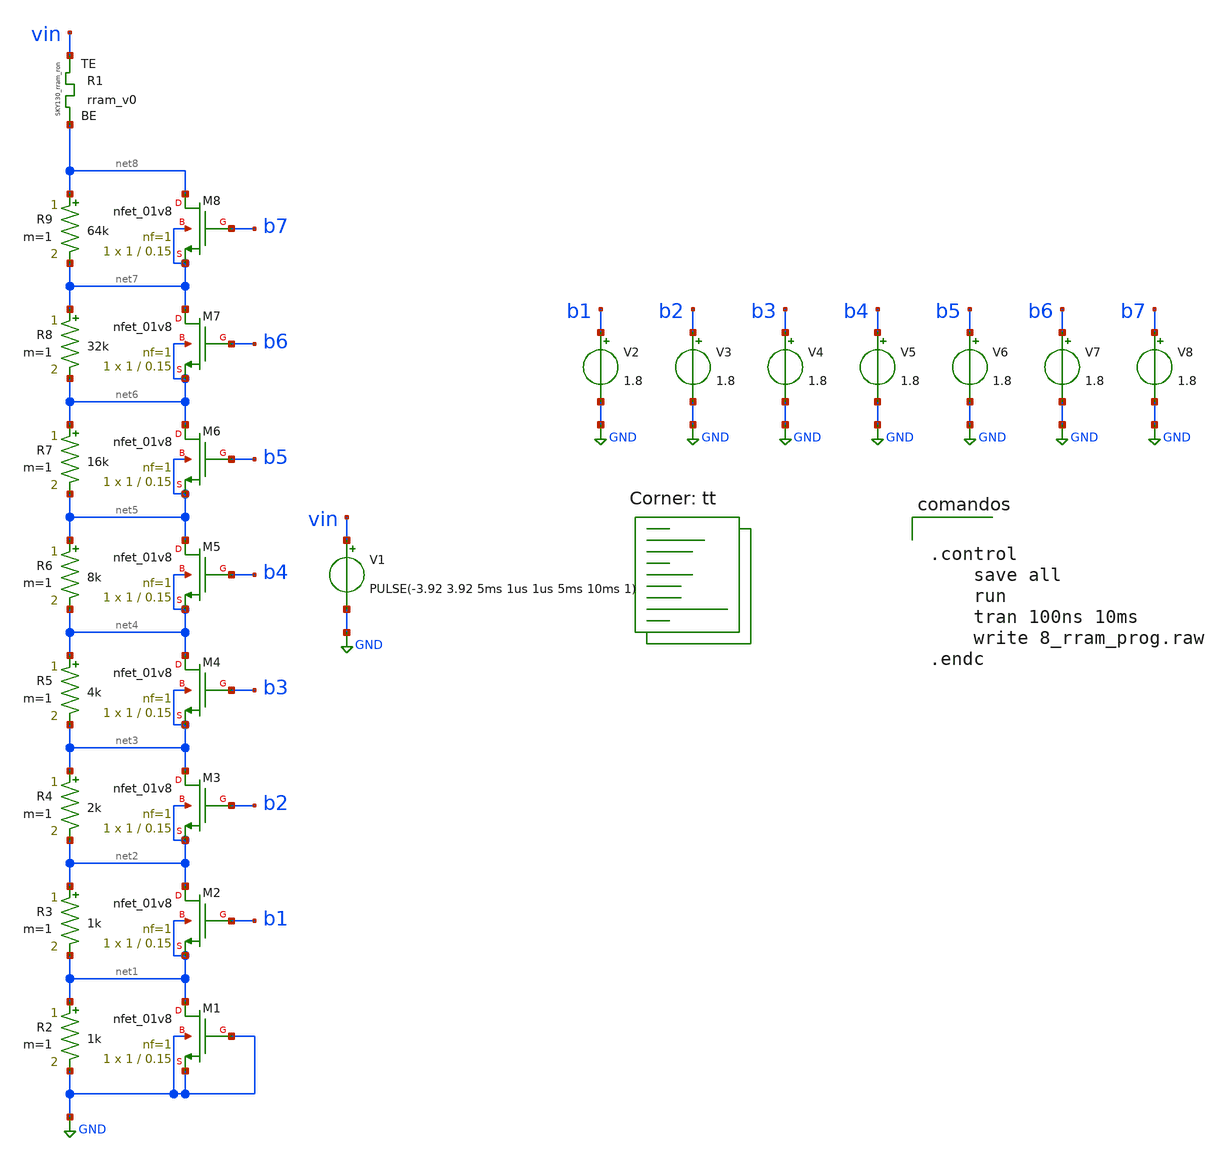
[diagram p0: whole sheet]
** sch_path: rram_programming/8_rram_prog.sch
**.subckt 8_rram_prog
V1 vin GND PULSE(-3.92 3.92 5ms 1us 1us 5ms 10ms 1)
XM1 net1 GND GND GND sky130_fd_pr__nfet_01v8 L=0.15 W=1 nf=1 ad='int((nf+1)/2) * W/nf * 0.29' as='int((nf+2)/2) * W/nf * 0.29'
+ pd='2*int((nf+1)/2) * (W/nf + 0.29)' ps='2*int((nf+2)/2) * (W/nf + 0.29)' nrd='0.29 / W' nrs='0.29 / W'
+ sa=0 sb=0 sd=0 mult=1 m=1
XR1 vin net8 rram_v0
R2 net1 GND 1k m=1
XM2 net2 b1 net1 net1 sky130_fd_pr__nfet_01v8 L=0.15 W=1 nf=1 ad='int((nf+1)/2) * W/nf * 0.29' as='int((nf+2)/2) * W/nf * 0.29'
+ pd='2*int((nf+1)/2) * (W/nf + 0.29)' ps='2*int((nf+2)/2) * (W/nf + 0.29)' nrd='0.29 / W' nrs='0.29 / W'
+ sa=0 sb=0 sd=0 mult=1 m=1
R3 net2 net1 1k m=1
XM3 net3 b2 net2 net2 sky130_fd_pr__nfet_01v8 L=0.15 W=1 nf=1 ad='int((nf+1)/2) * W/nf * 0.29' as='int((nf+2)/2) * W/nf * 0.29'
+ pd='2*int((nf+1)/2) * (W/nf + 0.29)' ps='2*int((nf+2)/2) * (W/nf + 0.29)' nrd='0.29 / W' nrs='0.29 / W'
+ sa=0 sb=0 sd=0 mult=1 m=1
R4 net3 net2 2k m=1
XM4 net4 b3 net3 net3 sky130_fd_pr__nfet_01v8 L=0.15 W=1 nf=1 ad='int((nf+1)/2) * W/nf * 0.29' as='int((nf+2)/2) * W/nf * 0.29'
+ pd='2*int((nf+1)/2) * (W/nf + 0.29)' ps='2*int((nf+2)/2) * (W/nf + 0.29)' nrd='0.29 / W' nrs='0.29 / W'
+ sa=0 sb=0 sd=0 mult=1 m=1
R5 net4 net3 4k m=1
XM5 net5 b4 net4 net4 sky130_fd_pr__nfet_01v8 L=0.15 W=1 nf=1 ad='int((nf+1)/2) * W/nf * 0.29' as='int((nf+2)/2) * W/nf * 0.29'
+ pd='2*int((nf+1)/2) * (W/nf + 0.29)' ps='2*int((nf+2)/2) * (W/nf + 0.29)' nrd='0.29 / W' nrs='0.29 / W'
+ sa=0 sb=0 sd=0 mult=1 m=1
R6 net5 net4 8k m=1
XM6 net6 b5 net5 net5 sky130_fd_pr__nfet_01v8 L=0.15 W=1 nf=1 ad='int((nf+1)/2) * W/nf * 0.29' as='int((nf+2)/2) * W/nf * 0.29'
+ pd='2*int((nf+1)/2) * (W/nf + 0.29)' ps='2*int((nf+2)/2) * (W/nf + 0.29)' nrd='0.29 / W' nrs='0.29 / W'
+ sa=0 sb=0 sd=0 mult=1 m=1
R7 net6 net5 16k m=1
XM7 net7 b6 net6 net6 sky130_fd_pr__nfet_01v8 L=0.15 W=1 nf=1 ad='int((nf+1)/2) * W/nf * 0.29' as='int((nf+2)/2) * W/nf * 0.29'
+ pd='2*int((nf+1)/2) * (W/nf + 0.29)' ps='2*int((nf+2)/2) * (W/nf + 0.29)' nrd='0.29 / W' nrs='0.29 / W'
+ sa=0 sb=0 sd=0 mult=1 m=1
R8 net7 net6 32k m=1
XM8 net8 b7 net7 net7 sky130_fd_pr__nfet_01v8 L=0.15 W=1 nf=1 ad='int((nf+1)/2) * W/nf * 0.29' as='int((nf+2)/2) * W/nf * 0.29'
+ pd='2*int((nf+1)/2) * (W/nf + 0.29)' ps='2*int((nf+2)/2) * (W/nf + 0.29)' nrd='0.29 / W' nrs='0.29 / W'
+ sa=0 sb=0 sd=0 mult=1 m=1
R9 net8 net7 64k m=1
V2 b1 GND 1.8
V3 b2 GND 1.8
V4 b3 GND 1.8
V5 b4 GND 1.8
V6 b5 GND 1.8
V7 b6 GND 1.8
V8 b7 GND 1.8
**** begin user architecture code
.lib $::SKYWATER_MODELS/sky130.lib.spice tt

** opencircuitdesign pdks install
.inc $::SKYWATER_MODELS/rram_v0.spice



.control
	save all
	run
	tran 100ns 10ms
	write 8_rram_prog.raw
.endc



**** end user architecture code
**.ends
.GLOBAL GND
.end
